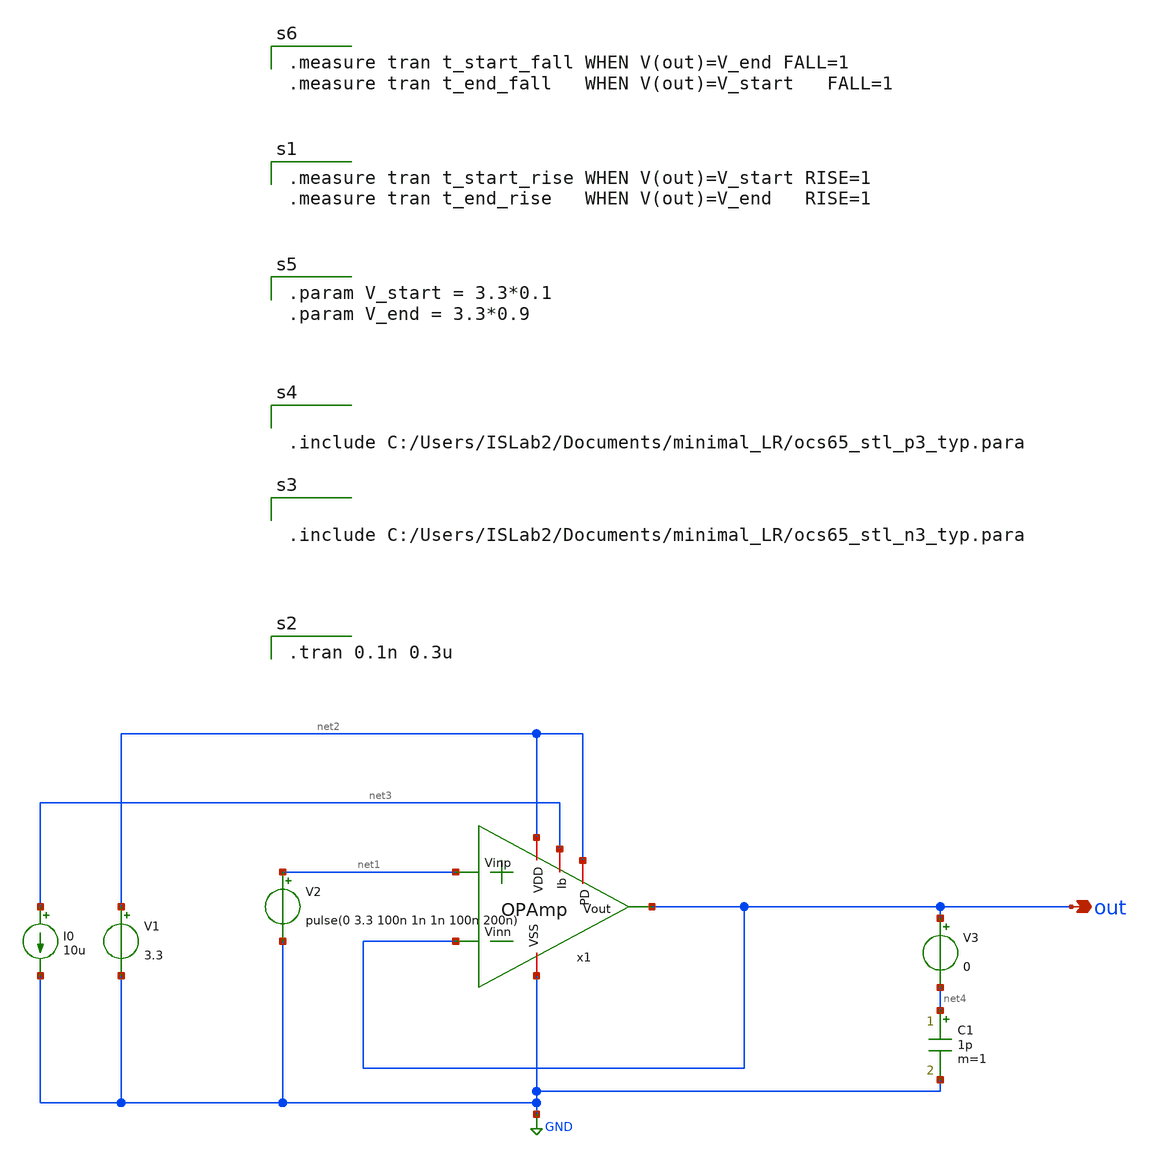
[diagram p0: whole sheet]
** sch_path: OPAmp_sim_SR.sch
**.subckt OPAmp_sim_SR out
*.opin out
V1 net2 GND 3.3
I0 net3 GND 10u
V2 net1 GND pulse(0 3.3 100n 1n 1n 100n 200n)
x1 net2 net3 out out net1 GND net2 OPAmp
C1 net4 GND 1p m=1
V3 out net4 0
**** begin user architecture code


.include C:/Users/ISLab2/Documents/minimal_LR/ocs65_stl_n3_typ.para



.include C:/Users/ISLab2/Documents/minimal_LR/ocs65_stl_p3_typ.para


.tran 0.1n 0.3u


.param V_start = 3.3*0.1
.param V_end = 3.3*0.9


.measure tran t_start_rise WHEN V(out)=V_start RISE=1
.measure tran t_end_rise   WHEN V(out)=V_end   RISE=1


.measure tran t_start_fall WHEN V(out)=V_end FALL=1
.measure tran t_end_fall   WHEN V(out)=V_start   FALL=1

**** end user architecture code
**.ends

* expanding   symbol:  OPAmp.sym # of pins=7
** sym_path: OPAmp.sym
** sch_path: OPAmp.sch
.subckt OPAmp VDD Ib Vout Vinn Vinp VSS PD
*.opin Vout
*.ipin Vinn
*.ipin Vinp
*.iopin Ib
*.iopin VDD
*.iopin VSS
*.iopin PD
M1 Ib Ib VDD VDD pch w=20u l=1u as=0 ps=0 ad=0 pd=0 m=1
M2 net1 Ib VDD VDD pch w=20u l=1u as=0 ps=0 ad=0 pd=0 m=3
M3 Vout Ib VDD VDD pch w=20u l=1u as=0 ps=0 ad=0 pd=0 m=10
M4 net3 net2 VSS VSS nch w=10u l=1u as=0 ps=0 ad=0 pd=0 m=1
M5 net2 Vinn net1 net1 pch w=20u l=1u as=0 ps=0 ad=0 pd=0 m=1
M6 net3 Vinp net1 net1 pch w=20u l=1u as=0 ps=0 ad=0 pd=0 m=1
M7 net2 net2 VSS VSS nch w=10u l=1u as=0 ps=0 ad=0 pd=0 m=1
M8 Vout net3 VSS VSS nch w=10u l=1u as=0 ps=0 ad=0 pd=0 m=10
C1 Vout net3 500f m=1
M9 Ib PD VDD VDD pch w=20u l=1u as=0 ps=0 ad=0 pd=0 m=1
M10 net3 net4 VSS VSS nch w=10u l=1u as=0 ps=0 ad=0 pd=0 m=1
x1 VDD net4 PD VSS INV
.ends


* expanding   symbol:  INV.sym # of pins=4
** sym_path: INV.sym
** sch_path: INV.sch
.subckt INV VDD OUT IN VSS
*.opin OUT
*.ipin IN
*.iopin VDD
*.iopin VSS
M2 OUT IN VDD VDD pch w=10u l=0.35u as=0 ps=0 ad=0 pd=0 m=1
M1 OUT IN VSS VSS nch w=5u l=0.35u as=0 ps=0 ad=0 pd=0 m=1
.ends

.GLOBAL GND
.end
